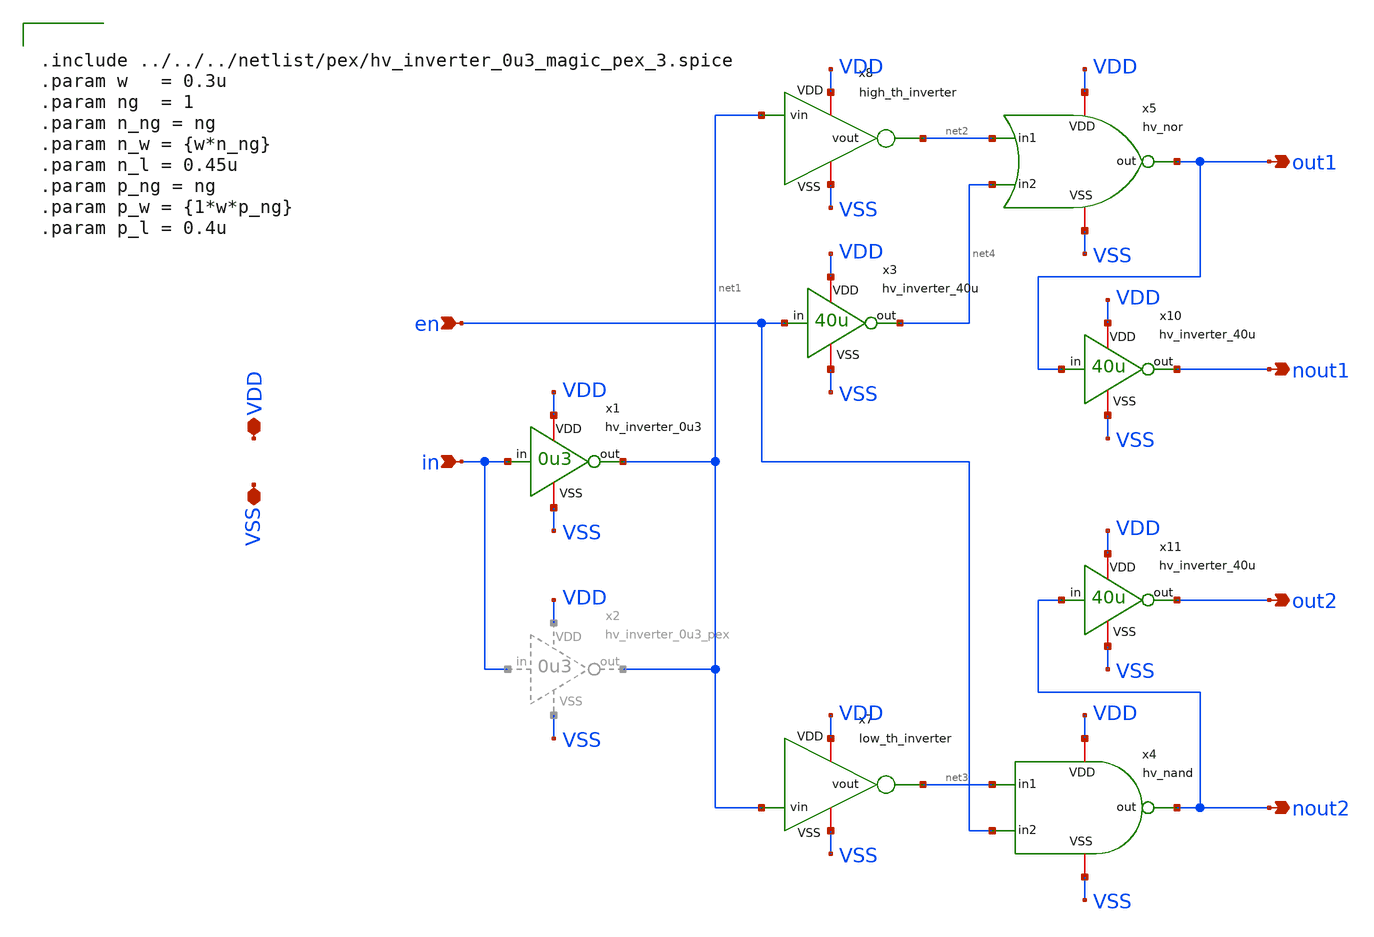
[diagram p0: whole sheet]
** sch_path: macros/heichips26_vcr/macros/switched_capacitor/schematic/xschem/pulse_shaper_en.sch
**.subckt pulse_shaper_en out1 nout1 out2 nout2 in VSS VDD en
*.opin out1
*.opin nout1
*.opin out2
*.opin nout2
*.ipin in
*.iopin VSS
*.iopin VDD
*.ipin en
x7 VDD net1 net3 VSS low_th_inverter
x8 VDD net1 net2 VSS high_th_inverter
x10 VDD out1 nout1 VSS hv_inverter_40u
x11 VDD nout2 out2 VSS hv_inverter_40u
x1 VDD in net1 VSS hv_inverter_0u3
x5 VDD net2 out1 net4 VSS hv_nor
x4 VDD net3 nout2 en VSS hv_nand
x3 VDD en net4 VSS hv_inverter_40u
**** begin user architecture code


.include ../../../netlist/pex/hv_inverter_0u3_magic_pex_3.spice
.param w   = 0.3u
.param ng  = 1
.param n_ng = ng
.param n_w = {w*n_ng}
.param n_l = 0.45u
.param p_ng = ng
.param p_w = {1*w*p_ng}
.param p_l = 0.4u


**** end user architecture code
**.ends

* expanding   symbol:  low_th_inverter.sym # of pins=4
** sym_path: macros/heichips26_vcr/macros/switched_capacitor/schematic/xschem/low_th_inverter.sym
** sch_path: macros/heichips26_vcr/macros/switched_capacitor/schematic/xschem/low_th_inverter.sch
.subckt low_th_inverter VDD vin vout VSS
*.ipin vin
*.iopin VDD
*.iopin VSS
*.opin vout
XM1 vout vin VSS VSS sg13_hv_nmos w={n_ng*n_w} l={n_l} ng={n_ng} m=1 mm_ok=1
XM2 vout vin VDD VDD sg13_hv_pmos w={p_ng*p_w} l={p_l} ng={n_ng} m=1 mm_ok=1
**** begin user architecture code


.param n_ng = 2
.param n_w = 1u
.param n_l = 0.45u
.param p_ng = 2
.param p_w = 1u
.param p_l = 0.4u


**** end user architecture code
.ends


* expanding   symbol:  high_th_inverter.sym # of pins=4
** sym_path: macros/heichips26_vcr/macros/switched_capacitor/schematic/xschem/high_th_inverter.sym
** sch_path: macros/heichips26_vcr/macros/switched_capacitor/schematic/xschem/high_th_inverter.sch
.subckt high_th_inverter VDD vin vout VSS
*.ipin vin
*.iopin VDD
*.iopin VSS
*.opin vout
XMdummy1 VSS VSS VSS VSS sg13_hv_nmos w=0.6u l=1.0u ng=2 m=1 mm_ok=1
XMdummy2 VDD VDD VDD VDD sg13_hv_pmos w=12.0u l=1.0u ng=2 m=1 mm_ok=1
XM1 vout vin VSS VSS sg13_hv_nmos w=6.0u l=1.0u ng=20 m=1 mm_ok=1
XM2 vout vin VDD VDD sg13_hv_pmos w=120.0u l=1.0u ng=20 m=1 mm_ok=1
.ends


* expanding   symbol:  hv_inverter_40u.sym # of pins=4
** sym_path: macros/heichips26_vcr/macros/switched_capacitor/schematic/xschem/hv_inverter_40u.sym
** sch_path: macros/heichips26_vcr/macros/switched_capacitor/schematic/xschem/hv_inverter_40u.sch
.subckt hv_inverter_40u VDD in out VSS
*.ipin in
*.iopin VDD
*.iopin VSS
*.opin out
XM2 out in VSS VSS sg13_hv_nmos w={n_w} l={n_l} ng={ng} m=1 mm_ok=1
XM3 out in VDD VDD sg13_hv_pmos w={p_w} l={p_l} ng={ng} m=1 mm_ok=1
**** begin user architecture code


.param w   = 10u
.param ng  = 4
.param n_ng = ng
.param n_w = {3u*n_ng}
.param n_l = 0.45u
.param p_ng = ng
.param p_w = {10u*p_ng}
.param p_l = 0.4u


**** end user architecture code
.ends


* expanding   symbol:  hv_inverter_0u3.sym # of pins=4
** sym_path: macros/heichips26_vcr/macros/switched_capacitor/schematic/xschem/hv_inverter_0u3.sym
** sch_path: macros/heichips26_vcr/macros/switched_capacitor/schematic/xschem/hv_inverter_0u3.sch
.subckt hv_inverter_0u3 VDD in out VSS
*.ipin in
*.iopin VDD
*.iopin VSS
*.opin out
XM2 out in VSS VSS sg13_hv_nmos w={n_w} l={n_l} ng={ng} m=1 mm_ok=1
XM3 out in VDD VDD sg13_hv_pmos w={p_w} l={p_l} ng={ng} m=1 mm_ok=1
**** begin user architecture code


.param w   = 0.3u
.param ng  = 1
.param n_ng = ng
.param n_w = {w*n_ng}
.param n_l = 0.45u
.param p_ng = ng
.param p_w = {1*w*p_ng}
.param p_l = 0.4u


**** end user architecture code
.ends


* expanding   symbol:  hv_nor.sym # of pins=5
** sym_path: macros/heichips26_vcr/macros/switched_capacitor/schematic/xschem/hv_nor.sym
** sch_path: macros/heichips26_vcr/macros/switched_capacitor/schematic/xschem/hv_nor.sch
.subckt hv_nor VDD in1 out in2 VSS
*.ipin in1
*.iopin VDD
*.iopin VSS
*.opin out
*.ipin in2
**** begin user architecture code


.param w   = 10u
.param ng  = 4
.param n_ng = ng
.param n_w = {3u*n_ng}
.param n_l = 0.45u
.param p_ng = ng
.param p_w = {10u*p_ng}
.param p_l = 0.4u


**** end user architecture code
XM2 out in1 VSS VSS sg13_hv_nmos w={n_w} l={n_l} ng={ng} m=1 mm_ok=1
XM3 net1 in2 VDD VDD sg13_hv_pmos w={p_w} l={p_l} ng={ng} m=1 mm_ok=1
XM1 out in2 VSS VSS sg13_hv_nmos w={n_w} l={n_l} ng={ng} m=1 mm_ok=1
XM4 out in1 net1 VDD sg13_hv_pmos w={p_w} l={p_l} ng={ng} m=1 mm_ok=1
.ends


* expanding   symbol:  hv_nand.sym # of pins=5
** sym_path: macros/heichips26_vcr/macros/switched_capacitor/schematic/xschem/hv_nand.sym
** sch_path: macros/heichips26_vcr/macros/switched_capacitor/schematic/xschem/hv_nand.sch
.subckt hv_nand VDD in1 out in2 VSS
*.ipin in1
*.iopin VDD
*.iopin VSS
*.opin out
*.ipin in2
**** begin user architecture code


.param w   = 10u
.param ng  = 4
.param n_ng = ng
.param n_w = {3u*n_ng}
.param n_l = 0.45u
.param p_ng = ng
.param p_w = {10u*p_ng}
.param p_l = 0.4u


**** end user architecture code
XM2 out in1 net1 VSS sg13_hv_nmos w={n_w} l={n_l} ng={ng} m=1 mm_ok=1
XM3 out in2 VDD VDD sg13_hv_pmos w={p_w} l={p_l} ng={ng} m=1 mm_ok=1
XM1 net1 in2 VSS VSS sg13_hv_nmos w={n_w} l={n_l} ng={ng} m=1 mm_ok=1
XM4 out in1 VDD VDD sg13_hv_pmos w={p_w} l={p_l} ng={ng} m=1 mm_ok=1
.ends

.end
